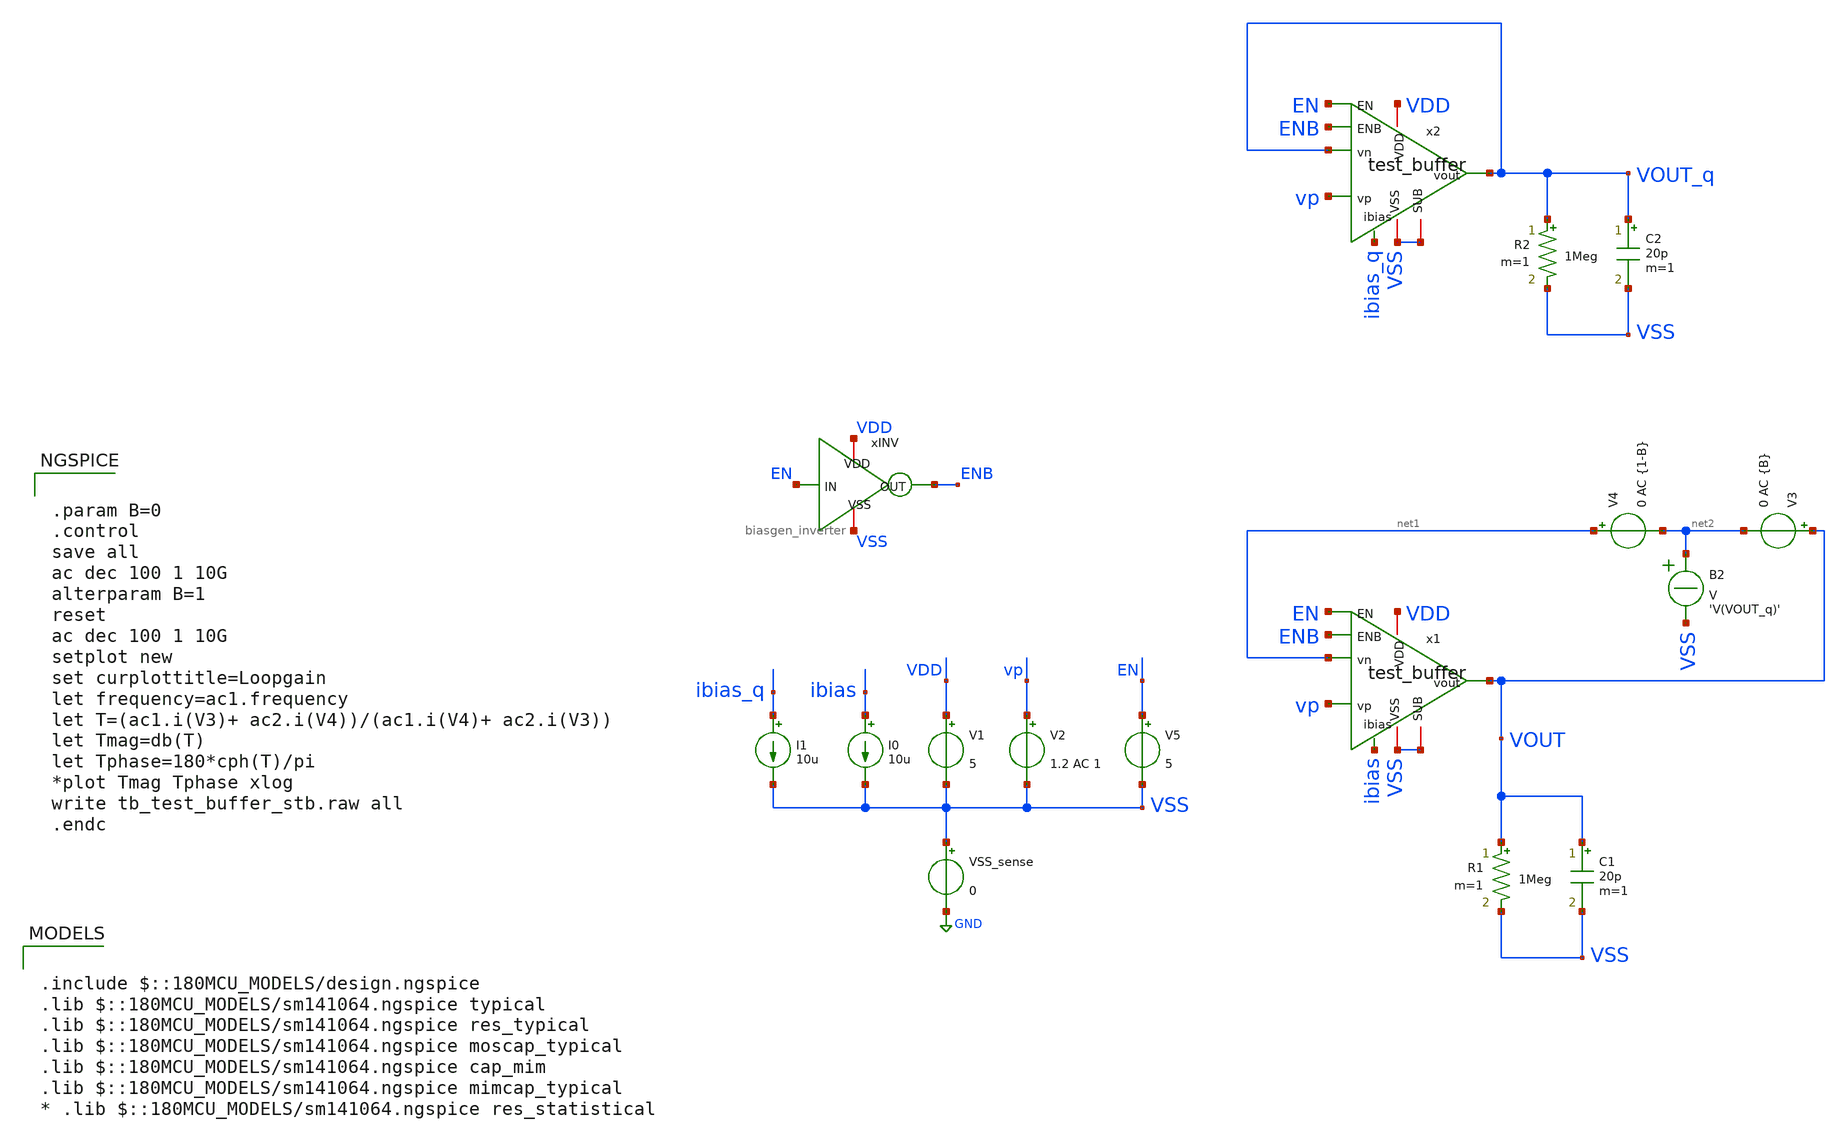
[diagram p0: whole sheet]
** sch_path: designs/libs/tb_test/tb_test_buffer_stb/tb_test_buffer_stb.sch
**.subckt tb_test_buffer_stb
V1 VDD VSS 5
V2 vp VSS 1.2 AC 1
VSS_sense VSS GND 0
I0 ibias VSS 10u
I1 ibias_q VSS 10u
xINV VDD EN ENB VSS biasgen_inverter
V4 net1 net2 0 AC {1-B}
B2 net2 VSS V = 'V(VOUT_q)'
V3 VOUT net2 0 AC {B}
V5 EN VSS 5
C1 VOUT VSS 20p m=1
R1 VOUT VSS 1Meg m=1
x1 VDD ibias net1 vp VOUT VSS EN ENB VSS test_buffer
C2 VOUT_q VSS 20p m=1
R2 VOUT_q VSS 1Meg m=1
x2 VDD ibias_q VOUT_q vp VOUT_q VSS EN ENB VSS test_buffer
**** begin user architecture code

.include $::180MCU_MODELS/design.ngspice
.lib $::180MCU_MODELS/sm141064.ngspice typical
.lib $::180MCU_MODELS/sm141064.ngspice res_typical
.lib $::180MCU_MODELS/sm141064.ngspice moscap_typical
.lib $::180MCU_MODELS/sm141064.ngspice cap_mim
.lib $::180MCU_MODELS/sm141064.ngspice mimcap_typical
* .lib $::180MCU_MODELS/sm141064.ngspice res_statistical



.param B=0
.control
save all
ac dec 100 1 10G
alterparam B=1
reset
ac dec 100 1 10G
setplot new
set curplottitle=Loopgain
let frequency=ac1.frequency
let T=(ac1.i(V3)+ ac2.i(V4))/(ac1.i(V4)+ ac2.i(V3))
let Tmag=db(T)
let Tphase=180*cph(T)/pi
*plot Tmag Tphase xlog
write tb_test_buffer_stb.raw all
.endc


**** end user architecture code
**.ends

* expanding   symbol:  libs/core_biasgen/biasgen_inverter/biasgen_inverter.sym # of pins=4
** sym_path: designs/libs/core_biasgen/biasgen_inverter/biasgen_inverter.sym
** sch_path: designs/libs/core_biasgen/biasgen_inverter/biasgen_inverter.sch
.subckt biasgen_inverter VDD IN OUT VSS
*.iopin VDD
*.iopin VSS
*.ipin IN
*.opin OUT
XMINV1 OUT IN VSS VSS nfet_05v0 L=0.60u W=0.50u nf=1 ad='int((nf+1)/2) * W/nf * 0.18u' as='int((nf+2)/2) * W/nf * 0.18u'
+ pd='2*int((nf+1)/2) * (W/nf + 0.18u)' ps='2*int((nf+2)/2) * (W/nf + 0.18u)' nrd='0.18u / W' nrs='0.18u / W'
+ sa=0 sb=0 sd=0 m=1
XMINV2 OUT IN VDD VDD pfet_05v0 L=0.50u W=0.60u nf=1 ad='int((nf+1)/2) * W/nf * 0.18u' as='int((nf+2)/2) * W/nf * 0.18u'
+ pd='2*int((nf+1)/2) * (W/nf + 0.18u)' ps='2*int((nf+2)/2) * (W/nf + 0.18u)' nrd='0.18u / W' nrs='0.18u / W'
+ sa=0 sb=0 sd=0 m=1
.ends


* expanding   symbol:  libs/core_test/test_buffer/test_buffer.sym # of pins=9
** sym_path: designs/libs/core_test/test_buffer/test_buffer.sym
** sch_path: designs/libs/core_test/test_buffer/test_buffer.sch
.subckt test_buffer VDD ibias vn vp vout VSS EN ENB SUB
*.ipin vn
*.ipin vp
*.opin vout
*.ipin ibias
*.iopin VDD
*.iopin VSS
*.ipin EN
*.ipin ENB
*.iopin SUB
XCM net1 vout_1st cap_nmos_03v3_b c_width=15u c_length=15u m=1
XMpref0 vpref vpref VDD VDD pfet_05v0 L=1u W=0.5u nf=1 ad='int((nf+1)/2) * W/nf * 0.18u' as='int((nf+2)/2) * W/nf * 0.18u'
+ pd='2*int((nf+1)/2) * (W/nf + 0.18u)' ps='2*int((nf+2)/2) * (W/nf + 0.18u)' nrd='0.18u / W' nrs='0.18u / W'
+ sa=0 sb=0 sd=0 m=10
XMnload0 vnload vnload VSS VSS nfet_05v0 L=2u W=0.5u nf=1 ad='int((nf+1)/2) * W/nf * 0.18u' as='int((nf+2)/2) * W/nf * 0.18u'
+ pd='2*int((nf+1)/2) * (W/nf + 0.18u)' ps='2*int((nf+2)/2) * (W/nf + 0.18u)' nrd='0.18u / W' nrs='0.18u / W'
+ sa=0 sb=0 sd=0 m=2
XMpref1 vptail vpref VDD VDD pfet_05v0 L=1u W=0.5u nf=1 ad='int((nf+1)/2) * W/nf * 0.18u' as='int((nf+2)/2) * W/nf * 0.18u'
+ pd='2*int((nf+1)/2) * (W/nf + 0.18u)' ps='2*int((nf+2)/2) * (W/nf + 0.18u)' nrd='0.18u / W' nrs='0.18u / W'
+ sa=0 sb=0 sd=0 m=2
XMpref2 net1 vpref VDD VDD pfet_05v0 L=1u W=0.5u nf=1 ad='int((nf+1)/2) * W/nf * 0.18u' as='int((nf+2)/2) * W/nf * 0.18u'
+ pd='2*int((nf+1)/2) * (W/nf + 0.18u)' ps='2*int((nf+2)/2) * (W/nf + 0.18u)' nrd='0.18u / W' nrs='0.18u / W'
+ sa=0 sb=0 sd=0 m=16
XMpdiff0 vnload vn vptail VDD pfet_05v0 L=1u W=2u nf=1 ad='int((nf+1)/2) * W/nf * 0.18u' as='int((nf+2)/2) * W/nf * 0.18u'
+ pd='2*int((nf+1)/2) * (W/nf + 0.18u)' ps='2*int((nf+2)/2) * (W/nf + 0.18u)' nrd='0.18u / W' nrs='0.18u / W'
+ sa=0 sb=0 sd=0 m=2
XMpdiff1 vout_1st vp vptail VDD pfet_05v0 L=1u W=2u nf=1 ad='int((nf+1)/2) * W/nf * 0.18u' as='int((nf+2)/2) * W/nf * 0.18u'
+ pd='2*int((nf+1)/2) * (W/nf + 0.18u)' ps='2*int((nf+2)/2) * (W/nf + 0.18u)' nrd='0.18u / W' nrs='0.18u / W'
+ sa=0 sb=0 sd=0 m=2
XMnload1 vout_1st vnload VSS VSS nfet_05v0 L=2u W=0.5u nf=1 ad='int((nf+1)/2) * W/nf * 0.18u' as='int((nf+2)/2) * W/nf * 0.18u'
+ pd='2*int((nf+1)/2) * (W/nf + 0.18u)' ps='2*int((nf+2)/2) * (W/nf + 0.18u)' nrd='0.18u / W' nrs='0.18u / W'
+ sa=0 sb=0 sd=0 m=2
XMncs net1 vout_1st VSS VSS nfet_05v0 L=2u W=0.5u nf=1 ad='int((nf+1)/2) * W/nf * 0.18u' as='int((nf+2)/2) * W/nf * 0.18u'
+ pd='2*int((nf+1)/2) * (W/nf + 0.18u)' ps='2*int((nf+2)/2) * (W/nf + 0.18u)' nrd='0.18u / W' nrs='0.18u / W'
+ sa=0 sb=0 sd=0 m=32
XMpref_dumm_L[3] VDD VDD VDD VDD pfet_05v0 L=1u W=0.5u nf=1 ad='int((nf+1)/2) * W/nf * 0.18u' as='int((nf+2)/2) * W/nf * 0.18u'
+ pd='2*int((nf+1)/2) * (W/nf + 0.18u)' ps='2*int((nf+2)/2) * (W/nf + 0.18u)' nrd='0.18u / W' nrs='0.18u / W'
+ sa=0 sb=0 sd=0 m=1
XMpref_dumm_L[2] VDD VDD VDD VDD pfet_05v0 L=1u W=0.5u nf=1 ad='int((nf+1)/2) * W/nf * 0.18u' as='int((nf+2)/2) * W/nf * 0.18u'
+ pd='2*int((nf+1)/2) * (W/nf + 0.18u)' ps='2*int((nf+2)/2) * (W/nf + 0.18u)' nrd='0.18u / W' nrs='0.18u / W'
+ sa=0 sb=0 sd=0 m=1
XMpref_dumm_L[1] VDD VDD VDD VDD pfet_05v0 L=1u W=0.5u nf=1 ad='int((nf+1)/2) * W/nf * 0.18u' as='int((nf+2)/2) * W/nf * 0.18u'
+ pd='2*int((nf+1)/2) * (W/nf + 0.18u)' ps='2*int((nf+2)/2) * (W/nf + 0.18u)' nrd='0.18u / W' nrs='0.18u / W'
+ sa=0 sb=0 sd=0 m=1
XMpref_dumm_L[0] VDD VDD VDD VDD pfet_05v0 L=1u W=0.5u nf=1 ad='int((nf+1)/2) * W/nf * 0.18u' as='int((nf+2)/2) * W/nf * 0.18u'
+ pd='2*int((nf+1)/2) * (W/nf + 0.18u)' ps='2*int((nf+2)/2) * (W/nf + 0.18u)' nrd='0.18u / W' nrs='0.18u / W'
+ sa=0 sb=0 sd=0 m=1
XMpref_dumm_TP[23] VDD VDD VDD VDD pfet_05v0 L=1u W=0.5u nf=1 ad='int((nf+1)/2) * W/nf * 0.18u' as='int((nf+2)/2) * W/nf * 0.18u'
+ pd='2*int((nf+1)/2) * (W/nf + 0.18u)' ps='2*int((nf+2)/2) * (W/nf + 0.18u)' nrd='0.18u / W' nrs='0.18u / W'
+ sa=0 sb=0 sd=0 m=1
XMpref_dumm_TP[22] VDD VDD VDD VDD pfet_05v0 L=1u W=0.5u nf=1 ad='int((nf+1)/2) * W/nf * 0.18u' as='int((nf+2)/2) * W/nf * 0.18u'
+ pd='2*int((nf+1)/2) * (W/nf + 0.18u)' ps='2*int((nf+2)/2) * (W/nf + 0.18u)' nrd='0.18u / W' nrs='0.18u / W'
+ sa=0 sb=0 sd=0 m=1
XMpref_dumm_TP[21] VDD VDD VDD VDD pfet_05v0 L=1u W=0.5u nf=1 ad='int((nf+1)/2) * W/nf * 0.18u' as='int((nf+2)/2) * W/nf * 0.18u'
+ pd='2*int((nf+1)/2) * (W/nf + 0.18u)' ps='2*int((nf+2)/2) * (W/nf + 0.18u)' nrd='0.18u / W' nrs='0.18u / W'
+ sa=0 sb=0 sd=0 m=1
XMpref_dumm_TP[20] VDD VDD VDD VDD pfet_05v0 L=1u W=0.5u nf=1 ad='int((nf+1)/2) * W/nf * 0.18u' as='int((nf+2)/2) * W/nf * 0.18u'
+ pd='2*int((nf+1)/2) * (W/nf + 0.18u)' ps='2*int((nf+2)/2) * (W/nf + 0.18u)' nrd='0.18u / W' nrs='0.18u / W'
+ sa=0 sb=0 sd=0 m=1
XMpref_dumm_TP[19] VDD VDD VDD VDD pfet_05v0 L=1u W=0.5u nf=1 ad='int((nf+1)/2) * W/nf * 0.18u' as='int((nf+2)/2) * W/nf * 0.18u'
+ pd='2*int((nf+1)/2) * (W/nf + 0.18u)' ps='2*int((nf+2)/2) * (W/nf + 0.18u)' nrd='0.18u / W' nrs='0.18u / W'
+ sa=0 sb=0 sd=0 m=1
XMpref_dumm_TP[18] VDD VDD VDD VDD pfet_05v0 L=1u W=0.5u nf=1 ad='int((nf+1)/2) * W/nf * 0.18u' as='int((nf+2)/2) * W/nf * 0.18u'
+ pd='2*int((nf+1)/2) * (W/nf + 0.18u)' ps='2*int((nf+2)/2) * (W/nf + 0.18u)' nrd='0.18u / W' nrs='0.18u / W'
+ sa=0 sb=0 sd=0 m=1
XMpref_dumm_TP[17] VDD VDD VDD VDD pfet_05v0 L=1u W=0.5u nf=1 ad='int((nf+1)/2) * W/nf * 0.18u' as='int((nf+2)/2) * W/nf * 0.18u'
+ pd='2*int((nf+1)/2) * (W/nf + 0.18u)' ps='2*int((nf+2)/2) * (W/nf + 0.18u)' nrd='0.18u / W' nrs='0.18u / W'
+ sa=0 sb=0 sd=0 m=1
XMpref_dumm_TP[16] VDD VDD VDD VDD pfet_05v0 L=1u W=0.5u nf=1 ad='int((nf+1)/2) * W/nf * 0.18u' as='int((nf+2)/2) * W/nf * 0.18u'
+ pd='2*int((nf+1)/2) * (W/nf + 0.18u)' ps='2*int((nf+2)/2) * (W/nf + 0.18u)' nrd='0.18u / W' nrs='0.18u / W'
+ sa=0 sb=0 sd=0 m=1
XMpref_dumm_TP[15] VDD VDD VDD VDD pfet_05v0 L=1u W=0.5u nf=1 ad='int((nf+1)/2) * W/nf * 0.18u' as='int((nf+2)/2) * W/nf * 0.18u'
+ pd='2*int((nf+1)/2) * (W/nf + 0.18u)' ps='2*int((nf+2)/2) * (W/nf + 0.18u)' nrd='0.18u / W' nrs='0.18u / W'
+ sa=0 sb=0 sd=0 m=1
XMpref_dumm_TP[14] VDD VDD VDD VDD pfet_05v0 L=1u W=0.5u nf=1 ad='int((nf+1)/2) * W/nf * 0.18u' as='int((nf+2)/2) * W/nf * 0.18u'
+ pd='2*int((nf+1)/2) * (W/nf + 0.18u)' ps='2*int((nf+2)/2) * (W/nf + 0.18u)' nrd='0.18u / W' nrs='0.18u / W'
+ sa=0 sb=0 sd=0 m=1
XMpref_dumm_TP[13] VDD VDD VDD VDD pfet_05v0 L=1u W=0.5u nf=1 ad='int((nf+1)/2) * W/nf * 0.18u' as='int((nf+2)/2) * W/nf * 0.18u'
+ pd='2*int((nf+1)/2) * (W/nf + 0.18u)' ps='2*int((nf+2)/2) * (W/nf + 0.18u)' nrd='0.18u / W' nrs='0.18u / W'
+ sa=0 sb=0 sd=0 m=1
XMpref_dumm_TP[12] VDD VDD VDD VDD pfet_05v0 L=1u W=0.5u nf=1 ad='int((nf+1)/2) * W/nf * 0.18u' as='int((nf+2)/2) * W/nf * 0.18u'
+ pd='2*int((nf+1)/2) * (W/nf + 0.18u)' ps='2*int((nf+2)/2) * (W/nf + 0.18u)' nrd='0.18u / W' nrs='0.18u / W'
+ sa=0 sb=0 sd=0 m=1
XMpref_dumm_TP[11] VDD VDD VDD VDD pfet_05v0 L=1u W=0.5u nf=1 ad='int((nf+1)/2) * W/nf * 0.18u' as='int((nf+2)/2) * W/nf * 0.18u'
+ pd='2*int((nf+1)/2) * (W/nf + 0.18u)' ps='2*int((nf+2)/2) * (W/nf + 0.18u)' nrd='0.18u / W' nrs='0.18u / W'
+ sa=0 sb=0 sd=0 m=1
XMpref_dumm_TP[10] VDD VDD VDD VDD pfet_05v0 L=1u W=0.5u nf=1 ad='int((nf+1)/2) * W/nf * 0.18u' as='int((nf+2)/2) * W/nf * 0.18u'
+ pd='2*int((nf+1)/2) * (W/nf + 0.18u)' ps='2*int((nf+2)/2) * (W/nf + 0.18u)' nrd='0.18u / W' nrs='0.18u / W'
+ sa=0 sb=0 sd=0 m=1
XMpref_dumm_TP[9] VDD VDD VDD VDD pfet_05v0 L=1u W=0.5u nf=1 ad='int((nf+1)/2) * W/nf * 0.18u' as='int((nf+2)/2) * W/nf * 0.18u'
+ pd='2*int((nf+1)/2) * (W/nf + 0.18u)' ps='2*int((nf+2)/2) * (W/nf + 0.18u)' nrd='0.18u / W' nrs='0.18u / W'
+ sa=0 sb=0 sd=0 m=1
XMpref_dumm_TP[8] VDD VDD VDD VDD pfet_05v0 L=1u W=0.5u nf=1 ad='int((nf+1)/2) * W/nf * 0.18u' as='int((nf+2)/2) * W/nf * 0.18u'
+ pd='2*int((nf+1)/2) * (W/nf + 0.18u)' ps='2*int((nf+2)/2) * (W/nf + 0.18u)' nrd='0.18u / W' nrs='0.18u / W'
+ sa=0 sb=0 sd=0 m=1
XMpref_dumm_TP[7] VDD VDD VDD VDD pfet_05v0 L=1u W=0.5u nf=1 ad='int((nf+1)/2) * W/nf * 0.18u' as='int((nf+2)/2) * W/nf * 0.18u'
+ pd='2*int((nf+1)/2) * (W/nf + 0.18u)' ps='2*int((nf+2)/2) * (W/nf + 0.18u)' nrd='0.18u / W' nrs='0.18u / W'
+ sa=0 sb=0 sd=0 m=1
XMpref_dumm_TP[6] VDD VDD VDD VDD pfet_05v0 L=1u W=0.5u nf=1 ad='int((nf+1)/2) * W/nf * 0.18u' as='int((nf+2)/2) * W/nf * 0.18u'
+ pd='2*int((nf+1)/2) * (W/nf + 0.18u)' ps='2*int((nf+2)/2) * (W/nf + 0.18u)' nrd='0.18u / W' nrs='0.18u / W'
+ sa=0 sb=0 sd=0 m=1
XMpref_dumm_TP[5] VDD VDD VDD VDD pfet_05v0 L=1u W=0.5u nf=1 ad='int((nf+1)/2) * W/nf * 0.18u' as='int((nf+2)/2) * W/nf * 0.18u'
+ pd='2*int((nf+1)/2) * (W/nf + 0.18u)' ps='2*int((nf+2)/2) * (W/nf + 0.18u)' nrd='0.18u / W' nrs='0.18u / W'
+ sa=0 sb=0 sd=0 m=1
XMpref_dumm_TP[4] VDD VDD VDD VDD pfet_05v0 L=1u W=0.5u nf=1 ad='int((nf+1)/2) * W/nf * 0.18u' as='int((nf+2)/2) * W/nf * 0.18u'
+ pd='2*int((nf+1)/2) * (W/nf + 0.18u)' ps='2*int((nf+2)/2) * (W/nf + 0.18u)' nrd='0.18u / W' nrs='0.18u / W'
+ sa=0 sb=0 sd=0 m=1
XMpref_dumm_TP[3] VDD VDD VDD VDD pfet_05v0 L=1u W=0.5u nf=1 ad='int((nf+1)/2) * W/nf * 0.18u' as='int((nf+2)/2) * W/nf * 0.18u'
+ pd='2*int((nf+1)/2) * (W/nf + 0.18u)' ps='2*int((nf+2)/2) * (W/nf + 0.18u)' nrd='0.18u / W' nrs='0.18u / W'
+ sa=0 sb=0 sd=0 m=1
XMpref_dumm_TP[2] VDD VDD VDD VDD pfet_05v0 L=1u W=0.5u nf=1 ad='int((nf+1)/2) * W/nf * 0.18u' as='int((nf+2)/2) * W/nf * 0.18u'
+ pd='2*int((nf+1)/2) * (W/nf + 0.18u)' ps='2*int((nf+2)/2) * (W/nf + 0.18u)' nrd='0.18u / W' nrs='0.18u / W'
+ sa=0 sb=0 sd=0 m=1
XMpref_dumm_TP[1] VDD VDD VDD VDD pfet_05v0 L=1u W=0.5u nf=1 ad='int((nf+1)/2) * W/nf * 0.18u' as='int((nf+2)/2) * W/nf * 0.18u'
+ pd='2*int((nf+1)/2) * (W/nf + 0.18u)' ps='2*int((nf+2)/2) * (W/nf + 0.18u)' nrd='0.18u / W' nrs='0.18u / W'
+ sa=0 sb=0 sd=0 m=1
XMpref_dumm_TP[0] VDD VDD VDD VDD pfet_05v0 L=1u W=0.5u nf=1 ad='int((nf+1)/2) * W/nf * 0.18u' as='int((nf+2)/2) * W/nf * 0.18u'
+ pd='2*int((nf+1)/2) * (W/nf + 0.18u)' ps='2*int((nf+2)/2) * (W/nf + 0.18u)' nrd='0.18u / W' nrs='0.18u / W'
+ sa=0 sb=0 sd=0 m=1
XMpenpref vpref EN VDD VDD pfet_05v0 L=0.5u W=1u nf=1 ad='int((nf+1)/2) * W/nf * 0.18u' as='int((nf+2)/2) * W/nf * 0.18u'
+ pd='2*int((nf+1)/2) * (W/nf + 0.18u)' ps='2*int((nf+2)/2) * (W/nf + 0.18u)' nrd='0.18u / W' nrs='0.18u / W'
+ sa=0 sb=0 sd=0 m=1
XMpenbias ibias ENB vpref VDD pfet_05v0 L=0.5u W=1u nf=1 ad='int((nf+1)/2) * W/nf * 0.18u' as='int((nf+2)/2) * W/nf * 0.18u'
+ pd='2*int((nf+1)/2) * (W/nf + 0.18u)' ps='2*int((nf+2)/2) * (W/nf + 0.18u)' nrd='0.18u / W' nrs='0.18u / W'
+ sa=0 sb=0 sd=0 m=5
XMnennref vnload ENB VSS VSS nfet_05v0 L=0.6u W=2u nf=1 ad='int((nf+1)/2) * W/nf * 0.18u' as='int((nf+2)/2) * W/nf * 0.18u'
+ pd='2*int((nf+1)/2) * (W/nf + 0.18u)' ps='2*int((nf+2)/2) * (W/nf + 0.18u)' nrd='0.18u / W' nrs='0.18u / W'
+ sa=0 sb=0 sd=0 m=1
XMnennref1 vout_1st ENB VSS VSS nfet_05v0 L=0.6u W=2u nf=1 ad='int((nf+1)/2) * W/nf * 0.18u' as='int((nf+2)/2) * W/nf * 0.18u'
+ pd='2*int((nf+1)/2) * (W/nf + 0.18u)' ps='2*int((nf+2)/2) * (W/nf + 0.18u)' nrd='0.18u / W' nrs='0.18u / W'
+ sa=0 sb=0 sd=0 m=1
* noconn SUB
XMpref3 net2 vpref VDD VDD pfet_05v0 L=1u W=0.5u nf=1 ad='int((nf+1)/2) * W/nf * 0.18u' as='int((nf+2)/2) * W/nf * 0.18u'
+ pd='2*int((nf+1)/2) * (W/nf + 0.18u)' ps='2*int((nf+2)/2) * (W/nf + 0.18u)' nrd='0.18u / W' nrs='0.18u / W'
+ sa=0 sb=0 sd=0 m=2
XMnbias0 net2 net2 VSS VSS nfet_05v0 L=2u W=0.5u nf=1 ad='int((nf+1)/2) * W/nf * 0.18u' as='int((nf+2)/2) * W/nf * 0.18u'
+ pd='2*int((nf+1)/2) * (W/nf + 0.18u)' ps='2*int((nf+2)/2) * (W/nf + 0.18u)' nrd='0.18u / W' nrs='0.18u / W'
+ sa=0 sb=0 sd=0 m=2
XMnbias1 vout net2 VSS VSS nfet_05v0 L=2u W=0.5u nf=1 ad='int((nf+1)/2) * W/nf * 0.18u' as='int((nf+2)/2) * W/nf * 0.18u'
+ pd='2*int((nf+1)/2) * (W/nf + 0.18u)' ps='2*int((nf+2)/2) * (W/nf + 0.18u)' nrd='0.18u / W' nrs='0.18u / W'
+ sa=0 sb=0 sd=0 m=64
XMnsf VDD net1 vout vout nfet_05v0 L=1u W=0.5u nf=1 ad='int((nf+1)/2) * W/nf * 0.18u' as='int((nf+2)/2) * W/nf * 0.18u'
+ pd='2*int((nf+1)/2) * (W/nf + 0.18u)' ps='2*int((nf+2)/2) * (W/nf + 0.18u)' nrd='0.18u / W' nrs='0.18u / W'
+ sa=0 sb=0 sd=0 m=64
XMnennref2 net2 ENB VSS VSS nfet_05v0 L=0.6u W=2u nf=1 ad='int((nf+1)/2) * W/nf * 0.18u' as='int((nf+2)/2) * W/nf * 0.18u'
+ pd='2*int((nf+1)/2) * (W/nf + 0.18u)' ps='2*int((nf+2)/2) * (W/nf + 0.18u)' nrd='0.18u / W' nrs='0.18u / W'
+ sa=0 sb=0 sd=0 m=1
XMnennref3 net1 ENB VSS VSS nfet_05v0 L=0.6u W=2u nf=1 ad='int((nf+1)/2) * W/nf * 0.18u' as='int((nf+2)/2) * W/nf * 0.18u'
+ pd='2*int((nf+1)/2) * (W/nf + 0.18u)' ps='2*int((nf+2)/2) * (W/nf + 0.18u)' nrd='0.18u / W' nrs='0.18u / W'
+ sa=0 sb=0 sd=0 m=1
.ends

.GLOBAL GND
.end
